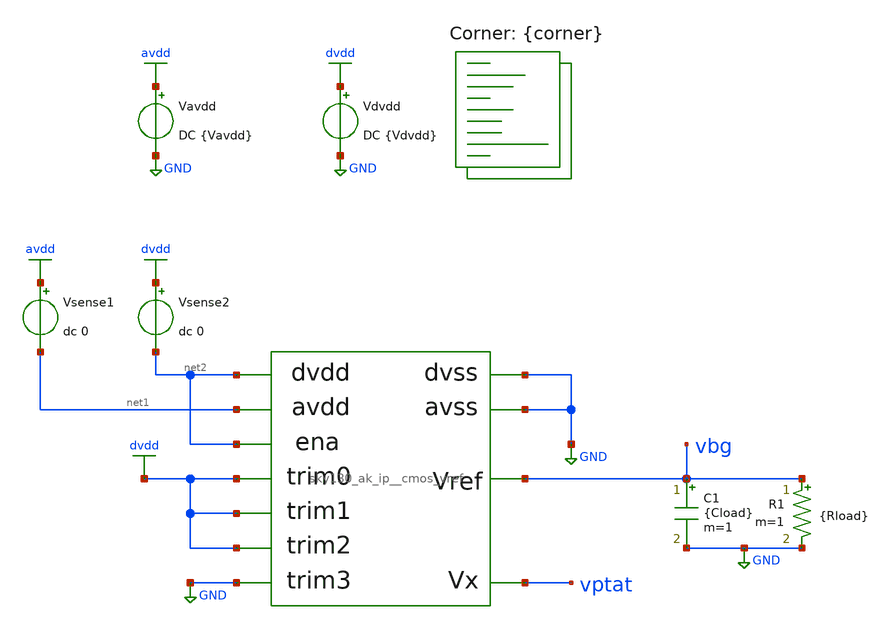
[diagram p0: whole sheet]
** sch_path: cace/tb_temp_coeff.sch
**.subckt tb_temp_coeff
Vavdd avdd GND DC {Vavdd}
X1 net1 GND dvdd vbg vptat dvdd dvdd GND net2 GND net2 sky130_ak_ip__cmos_vref
Vsense1 avdd net1 dc 0
Vdvdd dvdd GND DC {Vdvdd}
C1 vbg GND {Cload} m=1
Vsense2 dvdd net2 dc 0
R1 vbg GND {Rload} m=1
**** begin user architecture code


.option warn=1
.nodeset v(vbg)=1.2
.nodeset v(vptat)=0.1
.control
save vbg
dc TEMP -40 85 5

let temp_diff = {temperature|maximum}-{temperature|minimum}
let vref_diff = maximum(vbg)-minimum(vbg)
let vref_nom = (maximum(vbg)+minimum(vbg))/2
let temp_coeff = vref_diff/(vref_nom*temp_diff)

echo $&temp_coeff > {simpath}/{filename}_{N}.data

quit
.endc


.lib $::SKYWATER_MODELS/sky130.lib.spice {corner}
 .include $::SKYWATER_STDCELLS/sky130_fd_sc_hd.spice
**** end user architecture code
**.ends
.GLOBAL avdd
.GLOBAL GND
.GLOBAL dvdd
.end
